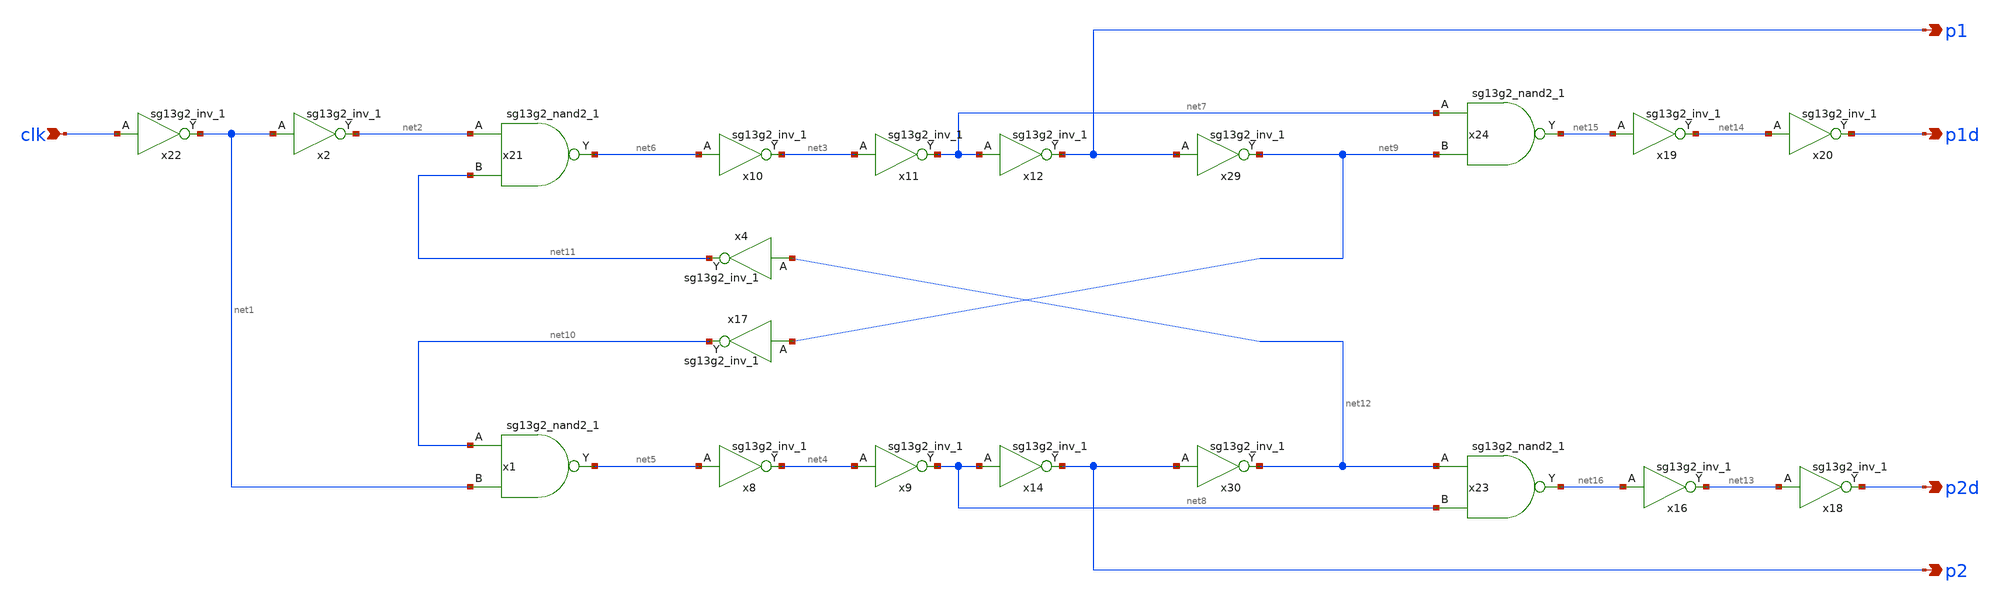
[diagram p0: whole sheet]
** sch_path: design/design_clkgen/clkgen.sch
**.subckt clkgen clk p1 p1d p2d p2
*.ipin clk
*.opin p1
*.opin p1d
*.opin p2d
*.opin p2
x21 net6 net2 net11 VDD VSS sg13g2_nand2_1
x22 net1 clk VDD VSS sg13g2_inv_1
x2 net2 net1 VDD VSS sg13g2_inv_1
x8 net4 net5 VDD VSS sg13g2_inv_1
x9 net8 net4 VDD VSS sg13g2_inv_1
x10 net3 net6 VDD VSS sg13g2_inv_1
x11 net7 net3 VDD VSS sg13g2_inv_1
x12 p1 net7 VDD VSS sg13g2_inv_1
x14 p2 net8 VDD VSS sg13g2_inv_1
x16 net13 net16 VDD VSS sg13g2_inv_1
x18 p2d net13 VDD VSS sg13g2_inv_1
x19 net14 net15 VDD VSS sg13g2_inv_1
x20 p1d net14 VDD VSS sg13g2_inv_1
x4 net11 net12 VDD VSS sg13g2_inv_1
x17 net10 net9 VDD VSS sg13g2_inv_1
x1 net5 net10 net1 VDD VSS sg13g2_nand2_1
x23 net16 net12 net8 VDD VSS sg13g2_nand2_1
x24 net15 net7 net9 VDD VSS sg13g2_nand2_1
x29 net9 p1 VDD VSS sg13g2_inv_1
x30 net12 p2 VDD VSS sg13g2_inv_1
**.ends

* expanding   symbol:  sg13g2_stdcells/sg13g2_nand2_1.sym # of pins=3
** sym_path: sg13g2_stdcells/sg13g2_nand2_1.sym
** sch_path: sg13g2_stdcells/sg13g2_nand2_1.sch
.subckt sg13g2_nand2_1 Y A B VDD VSS
*.iopin VDD
*.iopin VSS
*.ipin A
*.ipin B
*.opin Y
XM1 Y A net1 VSS sg13_lv_nmos w=740.00n l=130.00n ng=1 m=1 mm_ok=1
XM2 net1 B VSS VSS sg13_lv_nmos w=740.00n l=130.00n ng=1 m=1 mm_ok=1
XM3 Y A VDD VDD sg13_lv_pmos w=1.12u l=130.00n ng=1 m=1 mm_ok=1
XM4 Y B VDD VDD sg13_lv_pmos w=1.12u l=130.00n ng=1 m=1 mm_ok=1
.ends


* expanding   symbol:  sg13g2_stdcells/sg13g2_inv_1.sym # of pins=2
** sym_path: sg13g2_stdcells/sg13g2_inv_1.sym
** sch_path: sg13g2_stdcells/sg13g2_inv_1.sch
.subckt sg13g2_inv_1 Y A VDD VSS
*.opin Y
*.ipin A
*.iopin VDD
*.iopin VSS
XM1 Y A VSS VSS sg13_lv_nmos w=740.00n l=130.00n ng=1 m=1 mm_ok=1
XM2 Y A VDD VDD sg13_lv_pmos w=1.12u l=130.00n ng=1 m=1 mm_ok=1
.ends

.end
